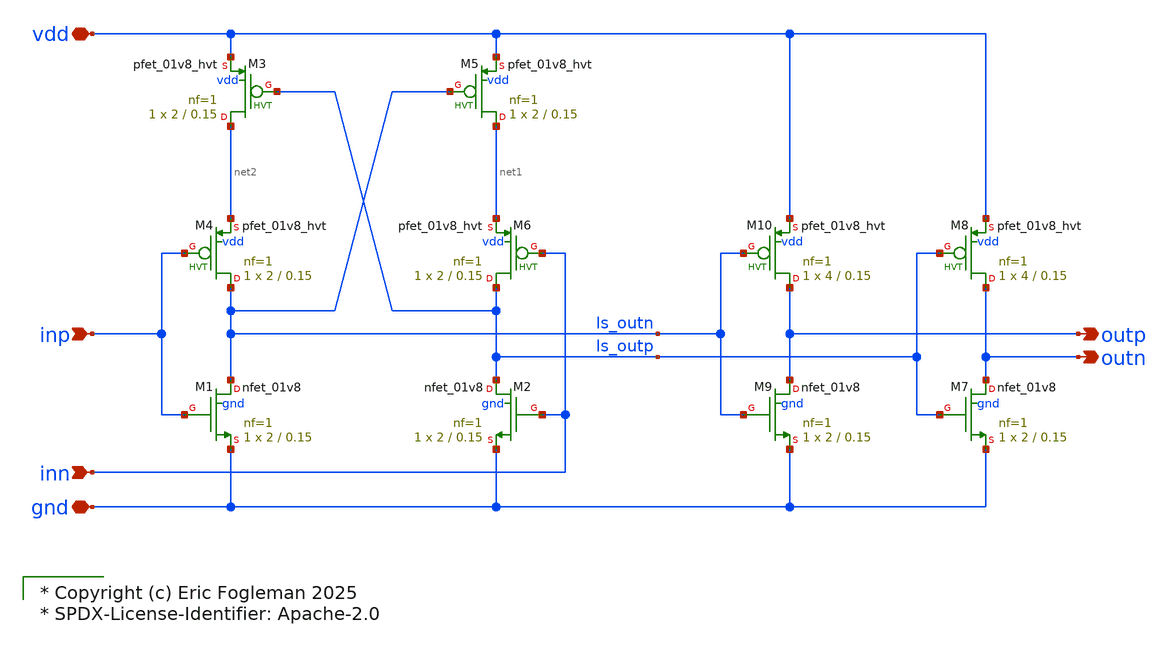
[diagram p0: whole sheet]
** sch_path: xschem/ejf_pll96_vco_ls.sch

* Copyright (c) Eric Fogleman 2025
* SPDX-License-Identifier: Apache-2.0

**.subckt ejf_pll96_vco_ls inp outn inn outp vdd gnd
*.ipin inp
*.opin outn
*.ipin inn
*.opin outp
*.iopin vdd
*.iopin gnd
XM5 net1 ls_outn vdd vdd sky130_fd_pr__pfet_01v8_hvt L=0.15 W=2 nf=1 ad='int((nf+1)/2) * W/nf * 0.29'
+ as='int((nf+2)/2) * W/nf * 0.29' pd='2*int((nf+1)/2) * (W/nf + 0.29)' ps='2*int((nf+2)/2) * (W/nf + 0.29)'
+ nrd='0.29 / W' nrs='0.29 / W' sa=0 sb=0 sd=0 mult=1 m=1
XM1 ls_outn inp gnd gnd sky130_fd_pr__nfet_01v8 L=0.15 W=2 nf=1 ad='int((nf+1)/2) * W/nf * 0.29' as='int((nf+2)/2) * W/nf * 0.29'
+ pd='2*int((nf+1)/2) * (W/nf + 0.29)' ps='2*int((nf+2)/2) * (W/nf + 0.29)' nrd='0.29 / W' nrs='0.29 / W'
+ sa=0 sb=0 sd=0 mult=1 m=1
XM2 ls_outp inn gnd gnd sky130_fd_pr__nfet_01v8 L=0.15 W=2 nf=1 ad='int((nf+1)/2) * W/nf * 0.29' as='int((nf+2)/2) * W/nf * 0.29'
+ pd='2*int((nf+1)/2) * (W/nf + 0.29)' ps='2*int((nf+2)/2) * (W/nf + 0.29)' nrd='0.29 / W' nrs='0.29 / W'
+ sa=0 sb=0 sd=0 mult=1 m=1
XM3 net2 ls_outp vdd vdd sky130_fd_pr__pfet_01v8_hvt L=0.15 W=2 nf=1 ad='int((nf+1)/2) * W/nf * 0.29'
+ as='int((nf+2)/2) * W/nf * 0.29' pd='2*int((nf+1)/2) * (W/nf + 0.29)' ps='2*int((nf+2)/2) * (W/nf + 0.29)'
+ nrd='0.29 / W' nrs='0.29 / W' sa=0 sb=0 sd=0 mult=1 m=1
XM4 ls_outn inp net2 vdd sky130_fd_pr__pfet_01v8_hvt L=0.15 W=2 nf=1 ad='int((nf+1)/2) * W/nf * 0.29'
+ as='int((nf+2)/2) * W/nf * 0.29' pd='2*int((nf+1)/2) * (W/nf + 0.29)' ps='2*int((nf+2)/2) * (W/nf + 0.29)'
+ nrd='0.29 / W' nrs='0.29 / W' sa=0 sb=0 sd=0 mult=1 m=1
XM6 ls_outp inn net1 vdd sky130_fd_pr__pfet_01v8_hvt L=0.15 W=2 nf=1 ad='int((nf+1)/2) * W/nf * 0.29'
+ as='int((nf+2)/2) * W/nf * 0.29' pd='2*int((nf+1)/2) * (W/nf + 0.29)' ps='2*int((nf+2)/2) * (W/nf + 0.29)'
+ nrd='0.29 / W' nrs='0.29 / W' sa=0 sb=0 sd=0 mult=1 m=1
XM7 outn ls_outp gnd gnd sky130_fd_pr__nfet_01v8 L=0.15 W=2 nf=1 ad='int((nf+1)/2) * W/nf * 0.29' as='int((nf+2)/2) * W/nf * 0.29'
+ pd='2*int((nf+1)/2) * (W/nf + 0.29)' ps='2*int((nf+2)/2) * (W/nf + 0.29)' nrd='0.29 / W' nrs='0.29 / W'
+ sa=0 sb=0 sd=0 mult=1 m=1
XM8 outn ls_outp vdd vdd sky130_fd_pr__pfet_01v8_hvt L=0.15 W=4 nf=1 ad='int((nf+1)/2) * W/nf * 0.29'
+ as='int((nf+2)/2) * W/nf * 0.29' pd='2*int((nf+1)/2) * (W/nf + 0.29)' ps='2*int((nf+2)/2) * (W/nf + 0.29)'
+ nrd='0.29 / W' nrs='0.29 / W' sa=0 sb=0 sd=0 mult=1 m=1
XM9 outp ls_outn gnd gnd sky130_fd_pr__nfet_01v8 L=0.15 W=2 nf=1 ad='int((nf+1)/2) * W/nf * 0.29' as='int((nf+2)/2) * W/nf * 0.29'
+ pd='2*int((nf+1)/2) * (W/nf + 0.29)' ps='2*int((nf+2)/2) * (W/nf + 0.29)' nrd='0.29 / W' nrs='0.29 / W'
+ sa=0 sb=0 sd=0 mult=1 m=1
XM10 outp ls_outn vdd vdd sky130_fd_pr__pfet_01v8_hvt L=0.15 W=4 nf=1 ad='int((nf+1)/2) * W/nf * 0.29'
+ as='int((nf+2)/2) * W/nf * 0.29' pd='2*int((nf+1)/2) * (W/nf + 0.29)' ps='2*int((nf+2)/2) * (W/nf + 0.29)'
+ nrd='0.29 / W' nrs='0.29 / W' sa=0 sb=0 sd=0 mult=1 m=1
**.ends
.end
